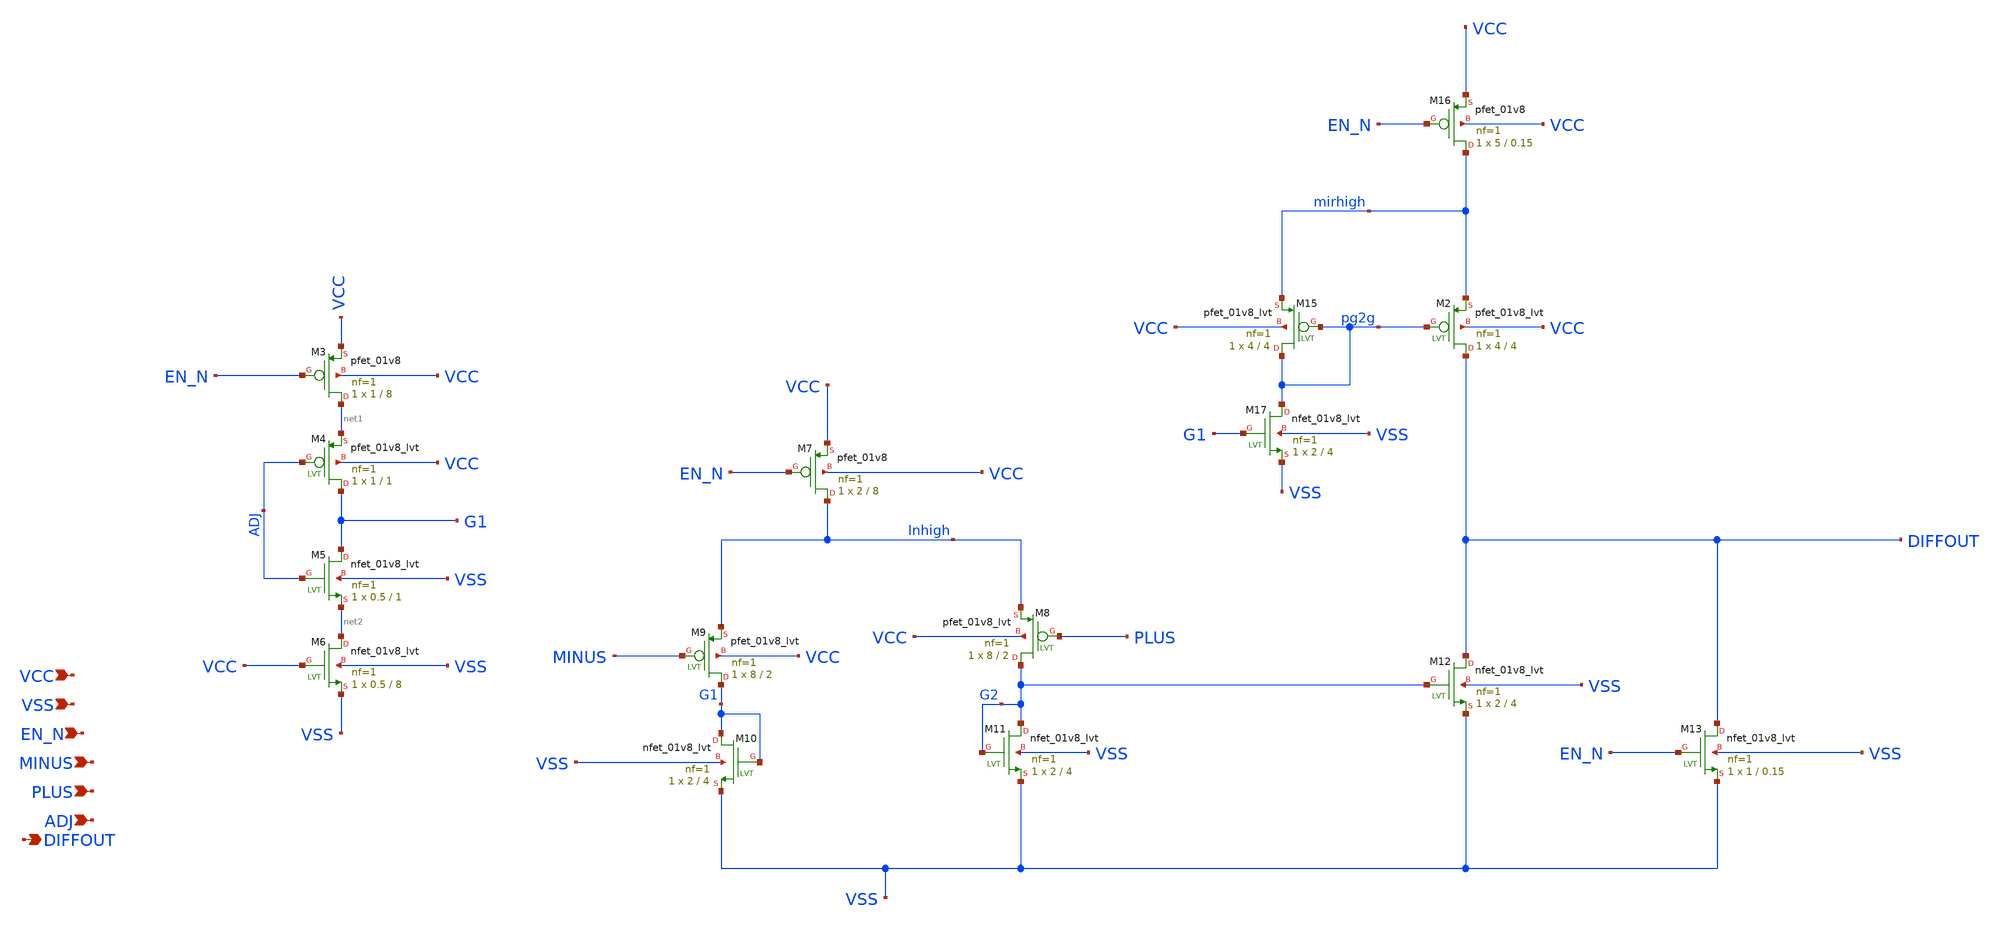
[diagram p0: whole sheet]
** sch_path: comparator.sch
* Copyright 2021 Stefan Frederik Schippers
* Licensed under the Apache License, Version 2.0 (the "License");
* you may not use this file except in compliance with the License.
* You may obtain a copy of the License at
* https://www.apache.org/licenses/LICENSE-2.0
* Unless required by applicable law or agreed to in writing, software
* distributed under the License is distributed on an "AS IS" BASIS,
* WITHOUT WARRANTIES OR CONDITIONS OF ANY KIND, either express or implied.
* See the License for the specific language governing permissions and
* limitations under the License.
**.subckt comparator VCC VSS EN_N MINUS PLUS ADJ DIFFOUT
*.ipin VCC
*.ipin VSS
*.ipin EN_N
*.ipin MINUS
*.ipin PLUS
*.ipin ADJ
*.opin DIFFOUT
XM3 net1 EN_N VCC VCC sky130_fd_pr__pfet_01v8 L=8 W=1 nf=1 ad='int((nf+1)/2) * W/nf * 0.29' as='int((nf+2)/2) * W/nf * 0.29'
+ pd='2*int((nf+1)/2) * (W/nf + 0.29)' ps='2*int((nf+2)/2) * (W/nf + 0.29)' nrd='0.29 / W' nrs='0.29 / W'
+ sa=0 sb=0 sd=0 mult=1 m=1
XM7 Inhigh EN_N VCC VCC sky130_fd_pr__pfet_01v8 L=8 W=2 nf=1 ad='int((nf+1)/2) * W/nf * 0.29' as='int((nf+2)/2) * W/nf * 0.29'
+ pd='2*int((nf+1)/2) * (W/nf + 0.29)' ps='2*int((nf+2)/2) * (W/nf + 0.29)' nrd='0.29 / W' nrs='0.29 / W'
+ sa=0 sb=0 sd=0 mult=1 m=1
XM16 mirhigh EN_N VCC VCC sky130_fd_pr__pfet_01v8 L=0.15 W=5 nf=1 ad='int((nf+1)/2) * W/nf * 0.29' as='int((nf+2)/2) * W/nf * 0.29'
+ pd='2*int((nf+1)/2) * (W/nf + 0.29)' ps='2*int((nf+2)/2) * (W/nf + 0.29)' nrd='0.29 / W' nrs='0.29 / W'
+ sa=0 sb=0 sd=0 mult=1 m=1
XM4 G1 ADJ net1 VCC sky130_fd_pr__pfet_01v8_lvt L=1 W=1 nf=1 ad='int((nf+1)/2) * W/nf * 0.29' as='int((nf+2)/2) * W/nf * 0.29'
+ pd='2*int((nf+1)/2) * (W/nf + 0.29)' ps='2*int((nf+2)/2) * (W/nf + 0.29)' nrd='0.29 / W' nrs='0.29 / W'
+ sa=0 sb=0 sd=0 mult=1 m=1
XM5 G1 ADJ net2 VSS sky130_fd_pr__nfet_01v8_lvt L=1 W=0.5 nf=1 ad='int((nf+1)/2) * W/nf * 0.29' as='int((nf+2)/2) * W/nf * 0.29'
+ pd='2*int((nf+1)/2) * (W/nf + 0.29)' ps='2*int((nf+2)/2) * (W/nf + 0.29)' nrd='0.29 / W' nrs='0.29 / W'
+ sa=0 sb=0 sd=0 mult=1 m=1
XM6 net2 VCC VSS VSS sky130_fd_pr__nfet_01v8_lvt L=8 W=0.5 nf=1 ad='int((nf+1)/2) * W/nf * 0.29' as='int((nf+2)/2) * W/nf * 0.29'
+ pd='2*int((nf+1)/2) * (W/nf + 0.29)' ps='2*int((nf+2)/2) * (W/nf + 0.29)' nrd='0.29 / W' nrs='0.29 / W'
+ sa=0 sb=0 sd=0 mult=1 m=1
XM9 G1 MINUS Inhigh VCC sky130_fd_pr__pfet_01v8_lvt L=2 W=8 nf=1 ad='int((nf+1)/2) * W/nf * 0.29' as='int((nf+2)/2) * W/nf * 0.29'
+ pd='2*int((nf+1)/2) * (W/nf + 0.29)' ps='2*int((nf+2)/2) * (W/nf + 0.29)' nrd='0.29 / W' nrs='0.29 / W'
+ sa=0 sb=0 sd=0 mult=1 m=1
XM8 G2 PLUS Inhigh VCC sky130_fd_pr__pfet_01v8_lvt L=2 W=8 nf=1 ad='int((nf+1)/2) * W/nf * 0.29' as='int((nf+2)/2) * W/nf * 0.29'
+ pd='2*int((nf+1)/2) * (W/nf + 0.29)' ps='2*int((nf+2)/2) * (W/nf + 0.29)' nrd='0.29 / W' nrs='0.29 / W'
+ sa=0 sb=0 sd=0 mult=1 m=1
XM11 G2 G2 VSS VSS sky130_fd_pr__nfet_01v8_lvt L=4 W=2 nf=1 ad='int((nf+1)/2) * W/nf * 0.29' as='int((nf+2)/2) * W/nf * 0.29'
+ pd='2*int((nf+1)/2) * (W/nf + 0.29)' ps='2*int((nf+2)/2) * (W/nf + 0.29)' nrd='0.29 / W' nrs='0.29 / W'
+ sa=0 sb=0 sd=0 mult=1 m=1
XM10 G1 G1 VSS VSS sky130_fd_pr__nfet_01v8_lvt L=4 W=2 nf=1 ad='int((nf+1)/2) * W/nf * 0.29' as='int((nf+2)/2) * W/nf * 0.29'
+ pd='2*int((nf+1)/2) * (W/nf + 0.29)' ps='2*int((nf+2)/2) * (W/nf + 0.29)' nrd='0.29 / W' nrs='0.29 / W'
+ sa=0 sb=0 sd=0 mult=1 m=1
XM12 DIFFOUT G2 VSS VSS sky130_fd_pr__nfet_01v8_lvt L=4 W=2 nf=1 ad='int((nf+1)/2) * W/nf * 0.29' as='int((nf+2)/2) * W/nf * 0.29'
+ pd='2*int((nf+1)/2) * (W/nf + 0.29)' ps='2*int((nf+2)/2) * (W/nf + 0.29)' nrd='0.29 / W' nrs='0.29 / W'
+ sa=0 sb=0 sd=0 mult=1 m=1
XM13 DIFFOUT EN_N VSS VSS sky130_fd_pr__nfet_01v8_lvt L=0.15 W=1 nf=1 ad='int((nf+1)/2) * W/nf * 0.29'
+ as='int((nf+2)/2) * W/nf * 0.29' pd='2*int((nf+1)/2) * (W/nf + 0.29)' ps='2*int((nf+2)/2) * (W/nf + 0.29)'
+ nrd='0.29 / W' nrs='0.29 / W' sa=0 sb=0 sd=0 mult=1 m=1
XM17 pg2g G1 VSS VSS sky130_fd_pr__nfet_01v8_lvt L=4 W=2 nf=1 ad='int((nf+1)/2) * W/nf * 0.29' as='int((nf+2)/2) * W/nf * 0.29'
+ pd='2*int((nf+1)/2) * (W/nf + 0.29)' ps='2*int((nf+2)/2) * (W/nf + 0.29)' nrd='0.29 / W' nrs='0.29 / W'
+ sa=0 sb=0 sd=0 mult=1 m=1
XM15 pg2g pg2g mirhigh VCC sky130_fd_pr__pfet_01v8_lvt L=4 W=4 nf=1 ad='int((nf+1)/2) * W/nf * 0.29'
+ as='int((nf+2)/2) * W/nf * 0.29' pd='2*int((nf+1)/2) * (W/nf + 0.29)' ps='2*int((nf+2)/2) * (W/nf + 0.29)'
+ nrd='0.29 / W' nrs='0.29 / W' sa=0 sb=0 sd=0 mult=1 m=1
XM2 DIFFOUT pg2g mirhigh VCC sky130_fd_pr__pfet_01v8_lvt L=4 W=4 nf=1 ad='int((nf+1)/2) * W/nf * 0.29'
+ as='int((nf+2)/2) * W/nf * 0.29' pd='2*int((nf+1)/2) * (W/nf + 0.29)' ps='2*int((nf+2)/2) * (W/nf + 0.29)'
+ nrd='0.29 / W' nrs='0.29 / W' sa=0 sb=0 sd=0 mult=1 m=1
**.ends
.end
